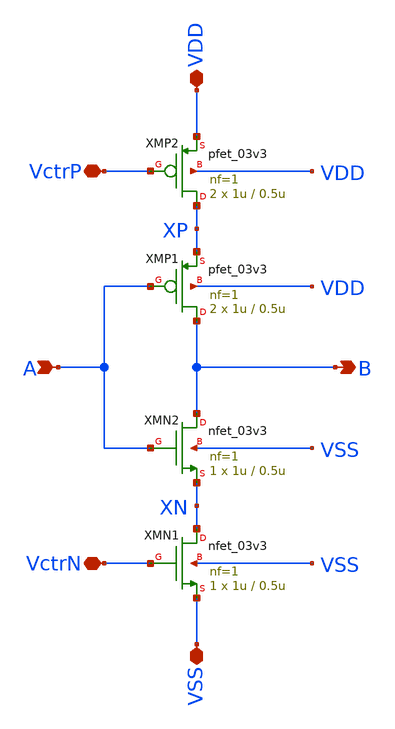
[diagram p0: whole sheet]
** sch_path: designs/integrator_inv/xschem/integrator_inv.sch
**.subckt integrator_inv B A VDD VSS VctrP VctrN
*.opin B
*.ipin A
*.iopin VDD
*.iopin VSS
*.iopin VctrP
*.iopin VctrN
XMN2 B A XN VSS nfet_03v3 L=0.5u W=1u nf=1 ad='int((nf+1)/2) * W/nf * 0.18u' as='int((nf+2)/2) * W/nf * 0.18u'
+ pd='2*int((nf+1)/2) * (W/nf + 0.18u)' ps='2*int((nf+2)/2) * (W/nf + 0.18u)' nrd='0.18u / W' nrs='0.18u / W'
+ sa=0 sb=0 sd=0 m=1
XMP1 B A XP VDD pfet_03v3 L=0.5u W=1u nf=1 ad='int((nf+1)/2) * W/nf * 0.18u' as='int((nf+2)/2) * W/nf * 0.18u'
+ pd='2*int((nf+1)/2) * (W/nf + 0.18u)' ps='2*int((nf+2)/2) * (W/nf + 0.18u)' nrd='0.18u / W' nrs='0.18u / W'
+ sa=0 sb=0 sd=0 m=2
XMP2 XP VctrP VDD VDD pfet_03v3 L=0.5u W=1u nf=1 ad='int((nf+1)/2) * W/nf * 0.18u' as='int((nf+2)/2) * W/nf * 0.18u'
+ pd='2*int((nf+1)/2) * (W/nf + 0.18u)' ps='2*int((nf+2)/2) * (W/nf + 0.18u)' nrd='0.18u / W' nrs='0.18u / W'
+ sa=0 sb=0 sd=0 m=2
XMN1 XN VctrN VSS VSS nfet_03v3 L=0.5u W=1u nf=1 ad='int((nf+1)/2) * W/nf * 0.18u' as='int((nf+2)/2) * W/nf * 0.18u'
+ pd='2*int((nf+1)/2) * (W/nf + 0.18u)' ps='2*int((nf+2)/2) * (W/nf + 0.18u)' nrd='0.18u / W' nrs='0.18u / W'
+ sa=0 sb=0 sd=0 m=1
**.ends
.end
